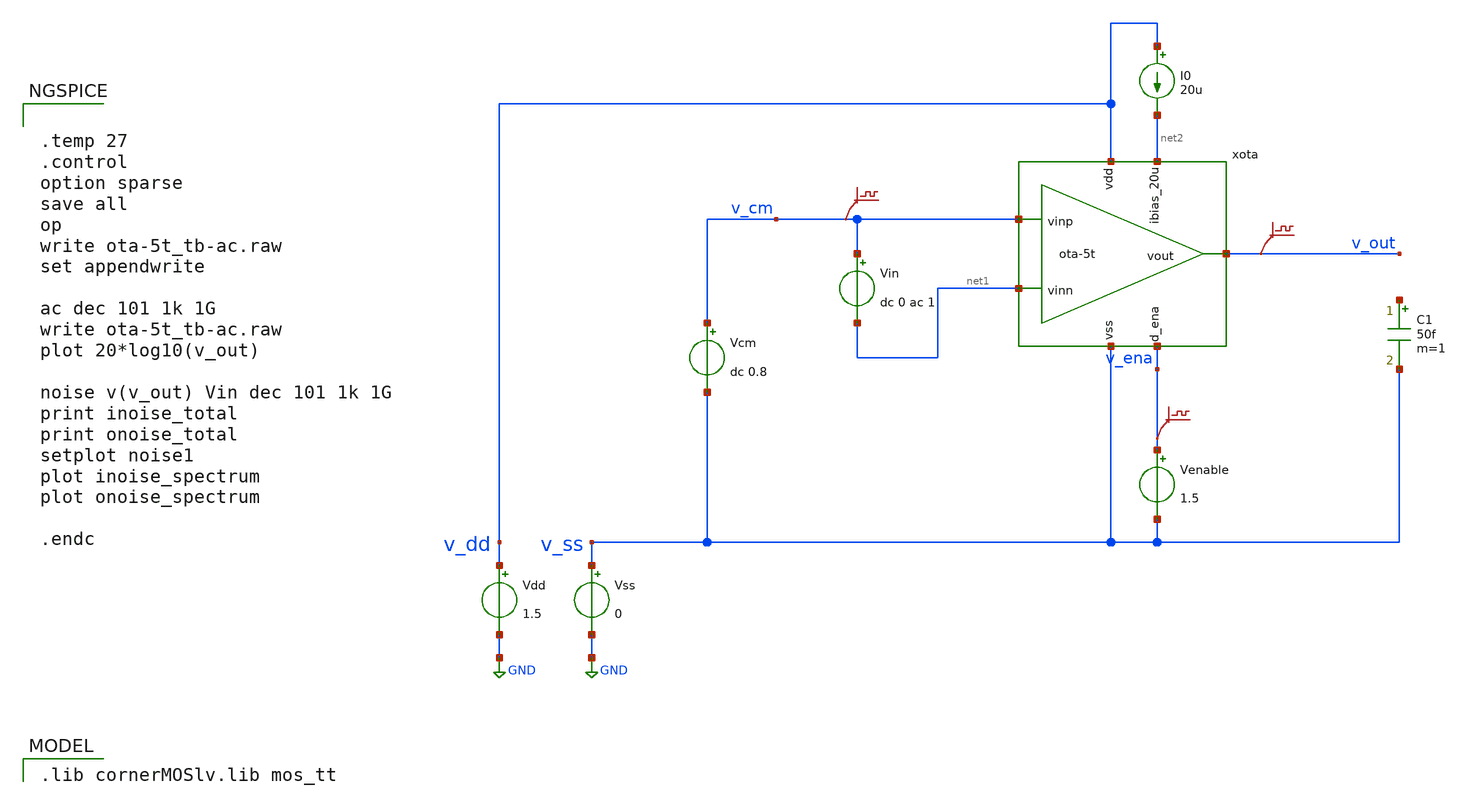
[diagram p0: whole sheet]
** sch_path: xschem/ota-5t_tb-noise.sch
* (c) 2024 H. Pretl, Apache-2.0 license
**.subckt ota-5t_tb-noise
Vdd v_dd GND 1.5
xota v_dd v_out v_cm net1 net2 v_ena v_ss ota-5t
Vss v_ss GND 0
C1 net3 v_ss 50f m=1
Vcm v_cm v_ss dc 0.8
I0 v_dd net2 20u
Venable v_ena v_ss 1.5
.save v(v_cm)
.save v(v_out)
.save v(v_ena)
Vin v_cm net1 dc 0 ac 1
**** begin user architecture code
 .lib cornerMOSlv.lib mos_tt



.temp 27
.control
option sparse
save all
op
write ota-5t_tb-ac.raw
set appendwrite

ac dec 101 1k 1G
write ota-5t_tb-ac.raw
plot 20*log10(v_out)

noise v(v_out) Vin dec 101 1k 1G
print inoise_total
print onoise_total
setplot noise1
plot inoise_spectrum
plot onoise_spectrum

.endc


**** end user architecture code
**.ends
.GLOBAL GND
.end
